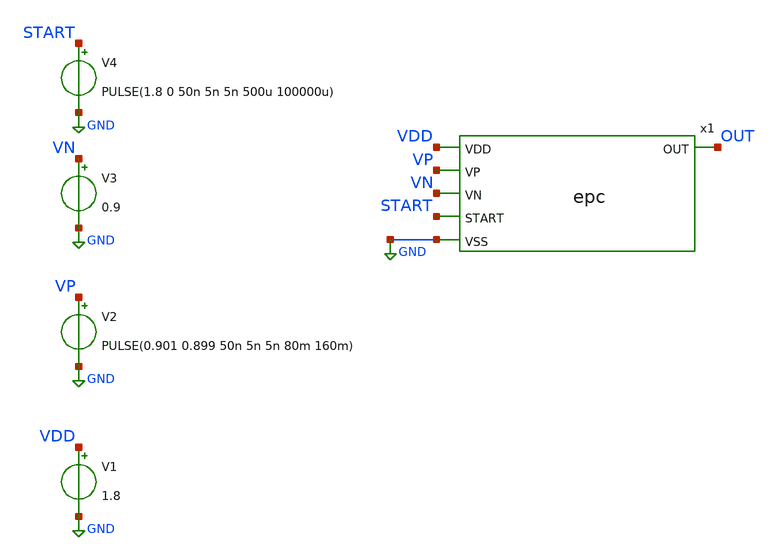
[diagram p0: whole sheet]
** sch_path: xschem/epc_tb.sch
**.subckt epc_tb
x1 VDD VP OUT VN START GND epc
V1 VDD GND 1.8
V2 VP GND PULSE(0.901 0.899 50n 5n 5n 80m 160m)
V3 VN GND 0.9
V4 START GND PULSE(1.8 0 50n 5n 5n 500u 100000u)
**** begin user architecture code

** opencircuitdesign pdks install
.lib $::SKYWATER_MODELS/sky130.lib.spice tt
.include /usr/local/share/pdk/sky130A/libs.ref/sky130_fd_sc_hd/spice/sky130_fd_sc_hd.spice



.option wnflag=0
.option savecurrents
.control
tran 1m 320m
plot V(vp) V(vn) V(out)
.endc

**** end user architecture code
**.ends
.GLOBAL GND
.end
